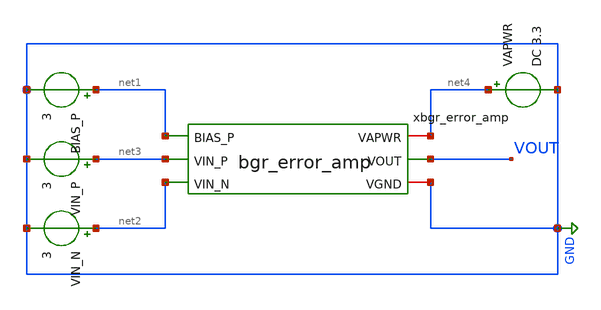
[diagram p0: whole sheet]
** sch_path: xschem/tb_bgr_error_amp.sch
**.subckt tb_bgr_error_amp
xbgr_error_amp net1 net4 net3 net2 VOUT GND bgr_error_amp
BIAS_P net1 GND 3
VIN_P net3 GND 3
VIN_N net2 GND 3
VAPWR net4 GND DC 3.3
**** begin user architecture code


.op


**** end user architecture code
**.ends

* expanding   symbol:  bgr_error_amp.sym # of pins=6
** sym_path: xschem/bgr_error_amp.sym
** sch_path: xschem/bgr_error_amp.sch
.subckt bgr_error_amp BIAS_P VAPWR VIN_P VIN_N VOUT VGND
*.ipin VIN_P
*.ipin VIN_N
*.ipin BIAS_P
*.iopin VAPWR
*.iopin VGND
*.opin VOUT
XMDIFF_P net1 VIN_P TAIL_P VAPWR pfet_03v3 L=0.28u W=0.22u nf=1 ad='int((nf+1)/2) * W/nf * 0.18u' as='int((nf+2)/2) * W/nf * 0.18u'
+ pd='2*int((nf+1)/2) * (W/nf + 0.18u)' ps='2*int((nf+2)/2) * (W/nf + 0.18u)' nrd='0.18u / W' nrs='0.18u / W'
+ sa=0 sb=0 sd=0 m=1
XMDIFF_N VOUT VIN_N TAIL_P VAPWR pfet_03v3 L=0.28u W=0.22u nf=1 ad='int((nf+1)/2) * W/nf * 0.18u' as='int((nf+2)/2) * W/nf * 0.18u'
+ pd='2*int((nf+1)/2) * (W/nf + 0.18u)' ps='2*int((nf+2)/2) * (W/nf + 0.18u)' nrd='0.18u / W' nrs='0.18u / W'
+ sa=0 sb=0 sd=0 m=1
XMTAIL TAIL_P BIAS_P VAPWR VAPWR pfet_03v3 L=0.28u W=0.22u nf=1 ad='int((nf+1)/2) * W/nf * 0.18u' as='int((nf+2)/2) * W/nf * 0.18u'
+ pd='2*int((nf+1)/2) * (W/nf + 0.18u)' ps='2*int((nf+2)/2) * (W/nf + 0.18u)' nrd='0.18u / W' nrs='0.18u / W'
+ sa=0 sb=0 sd=0 m=1
XMLOAD_REF net1 net1 VGND VGND nfet_03v3 L=0.28u W=0.22u nf=1 ad='int((nf+1)/2) * W/nf * 0.18u' as='int((nf+2)/2) * W/nf * 0.18u'
+ pd='2*int((nf+1)/2) * (W/nf + 0.18u)' ps='2*int((nf+2)/2) * (W/nf + 0.18u)' nrd='0.18u / W' nrs='0.18u / W'
+ sa=0 sb=0 sd=0 m=1
XMLOAD_OUT VOUT net1 VGND VGND nfet_03v3 L=0.28u W=0.22u nf=1 ad='int((nf+1)/2) * W/nf * 0.18u' as='int((nf+2)/2) * W/nf * 0.18u'
+ pd='2*int((nf+1)/2) * (W/nf + 0.18u)' ps='2*int((nf+2)/2) * (W/nf + 0.18u)' nrd='0.18u / W' nrs='0.18u / W'
+ sa=0 sb=0 sd=0 m=1
.ends

.GLOBAL GND
.end
